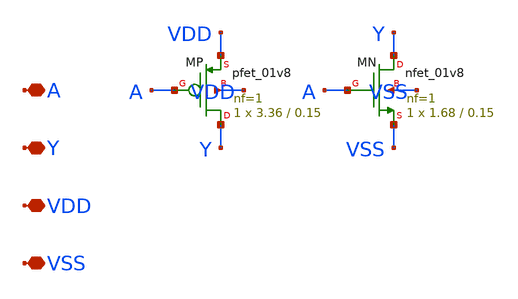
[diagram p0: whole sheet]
** sch_path: design/compiler/cells/sram_wldrv.sch
**.subckt sram_wldrv A Y VDD VSS
*.iopin A
*.iopin Y
*.iopin VDD
*.iopin VSS
XMP Y A VDD VDD sky130_fd_pr__pfet_01v8 L=0.15 W=3.36 nf=1 ad=0.9744 as=0.9744 pd=7.3 ps=7.3
+ nrd=0.08631 nrs=0.08631 sa=0 sb=0 sd=0 mult=1 m=1
XMN Y A VSS VSS sky130_fd_pr__nfet_01v8 L=0.15 W=1.68 nf=1 ad=0.4872 as=0.4872 pd=3.94 ps=3.94
+ nrd=0.1726 nrs=0.1726 sa=0 sb=0 sd=0 mult=1 m=1
**.ends
.end
